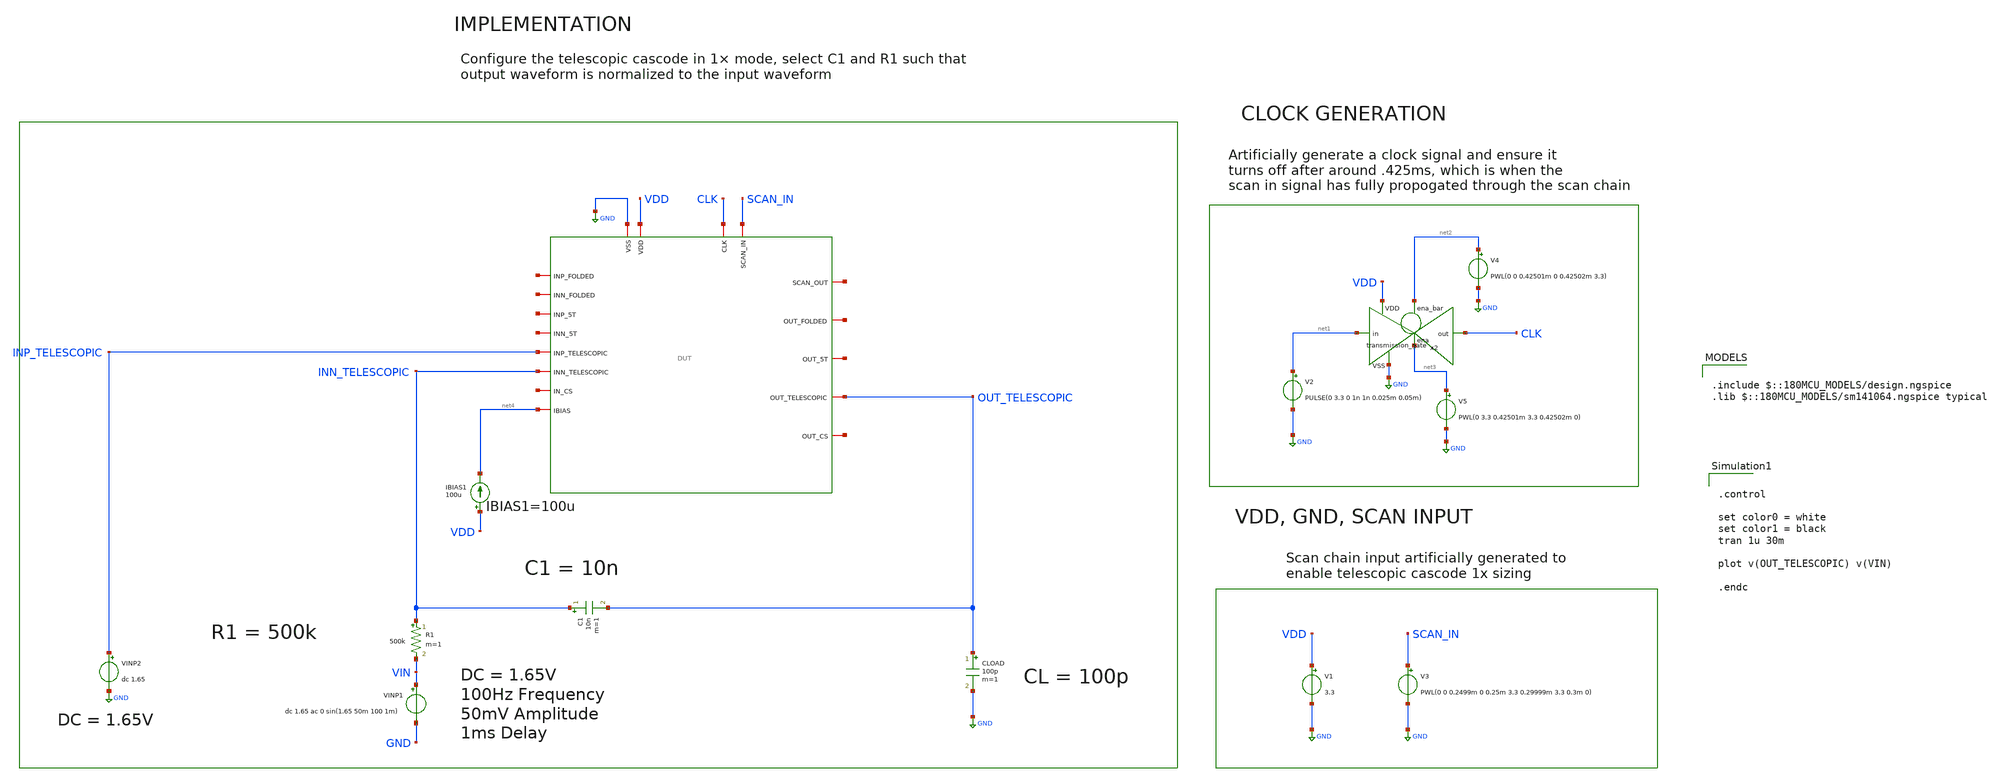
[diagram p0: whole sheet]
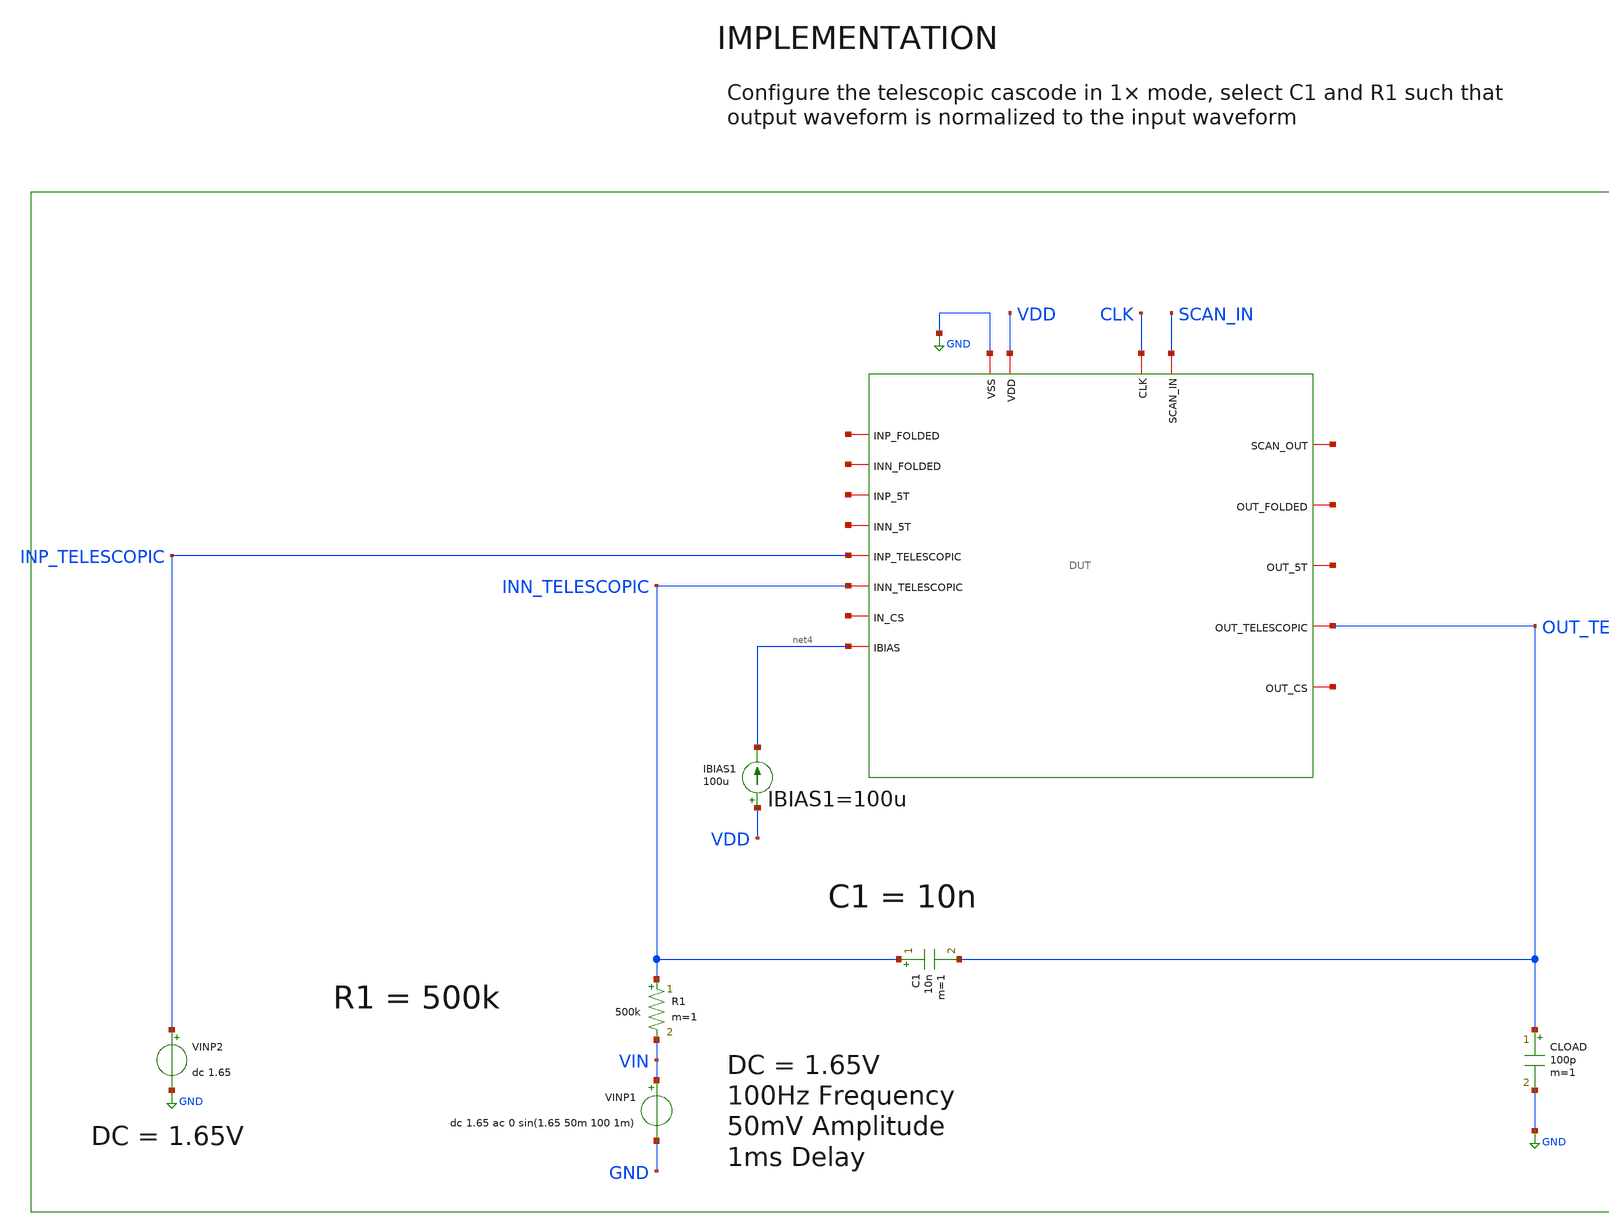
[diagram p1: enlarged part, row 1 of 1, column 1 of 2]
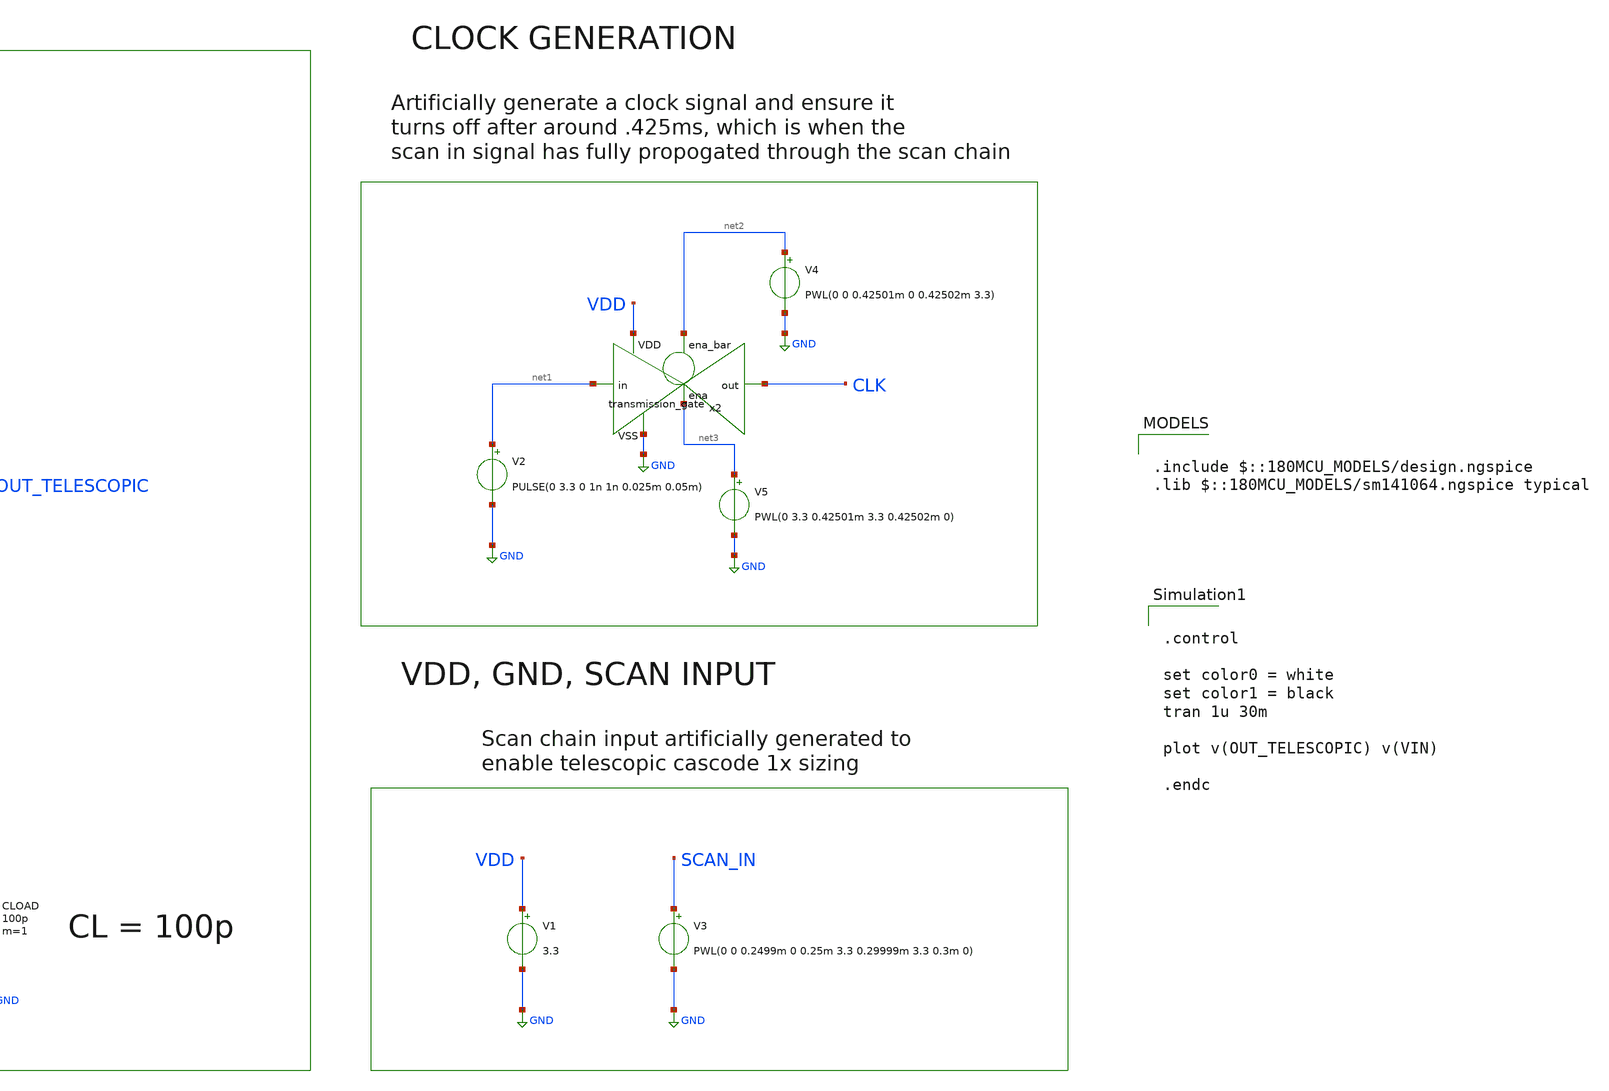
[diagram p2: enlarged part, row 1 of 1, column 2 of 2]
** sch_path: designs/libs/core_tb/mpg/ota_telescopic/integrator.sch
**.subckt integrator
V3 SCAN_IN GND PWL(0 0 0.2499m 0 0.25m 3.3 0.29999m 3.3 0.3m 0)
V1 VDD GND 3.3
V2 net1 GND PULSE(0 3.3 0 1n 1n 0.025m 0.05m)
x2 net2 VDD CLK net1 GND net3 transmission_gate
V4 net2 GND PWL(0 0 0.42501m 0 0.42502m 3.3)
V5 net3 GND PWL(0 3.3 0.42501m 3.3 0.42502m 0)
IBIAS1 VDD net4 100u
CLOAD OUT_TELESCOPIC GND 100p m=1
x1 CLK net5 SCAN_IN GND VDD net6 net7 net8 net4 net9 net10 net11 INP_TELESCOPIC OUT_TELESCOPIC net12
+ net13 INN_TELESCOPIC DUT
VINP1 VIN GND dc 1.65 ac 0 sin(1.65 50m 100 1m)
C1 INN_TELESCOPIC OUT_TELESCOPIC 10n m=1
R1 INN_TELESCOPIC VIN 500k m=1
VINP2 INP_TELESCOPIC GND dc 1.65
**** begin user architecture code

.include $::180MCU_MODELS/design.ngspice
.lib $::180MCU_MODELS/sm141064.ngspice typical



.control

set color0 = white
set color1 = black
tran 1u 30m

plot v(OUT_TELESCOPIC) v(VIN)

.endc

**** end user architecture code
**.ends
.GLOBAL GND
.end
